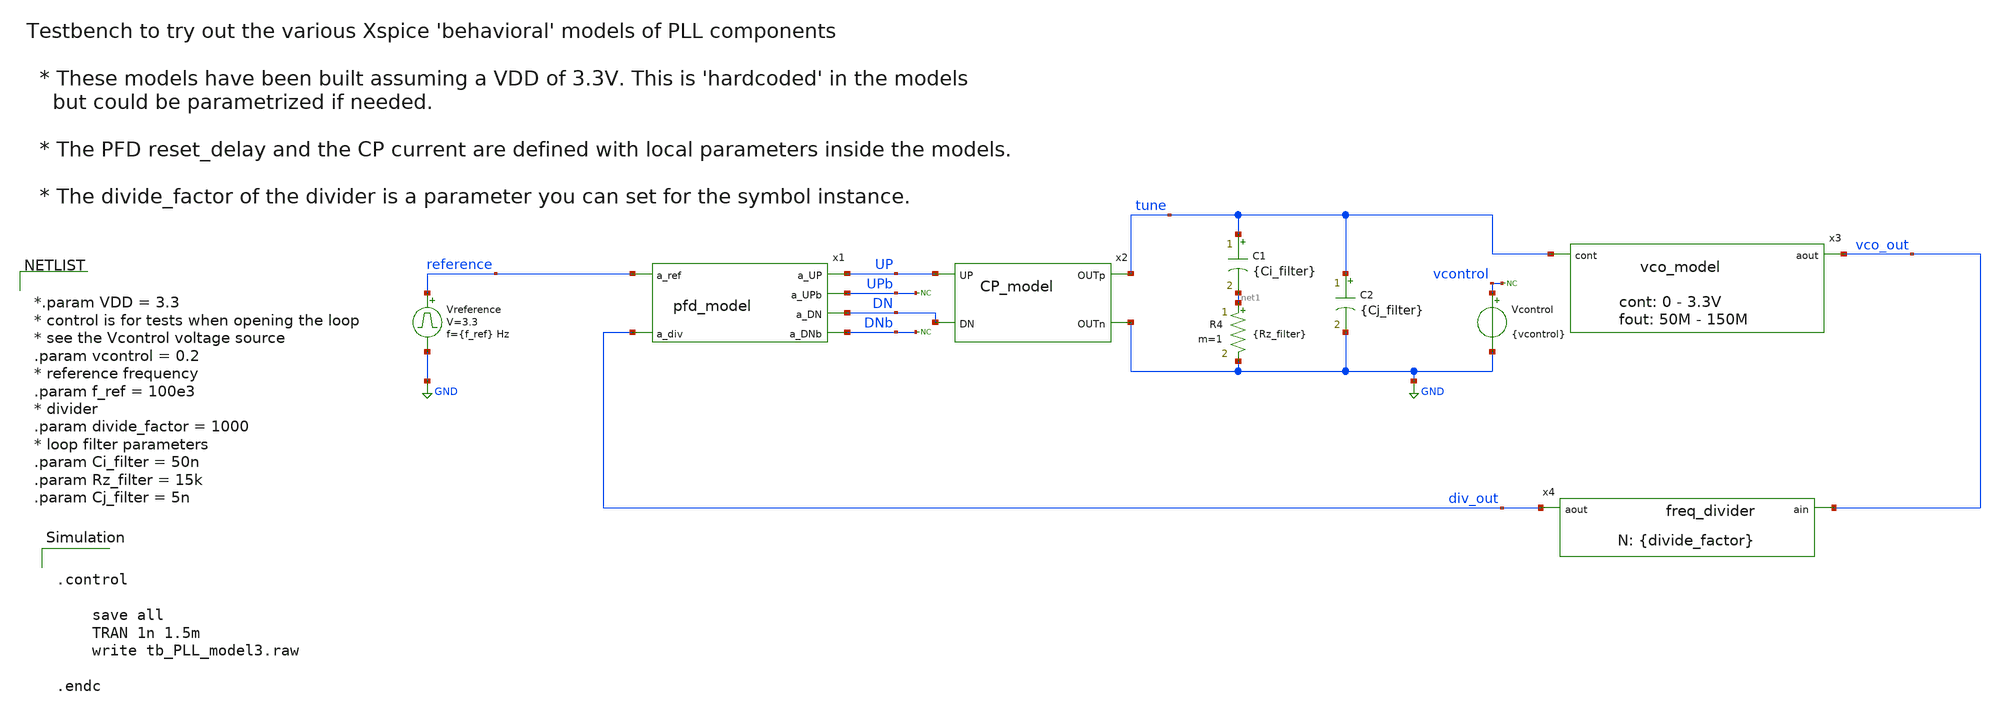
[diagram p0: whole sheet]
** sch_path: designs/libs/tb_pll/tb_PLL_IDEAL_model.sch
**.subckt tb_PLL_IDEAL_model
Vcontrol vcontrol GND {vcontrol}
Vreference reference GND pulse 0 3.3 '0.495/ {f_ref} ' '0.01/{f_ref} ' '0.01/{f_ref} ' '0.49/{f_ref} '
+ '1/{f_ref} '
C1 tune net1 {Ci_filter} m=1
R4 net1 GND {Rz_filter} m=1
* noconn vcontrol
* noconn UPb
* noconn DNb
C2 tune GND {Cj_filter} m=1
x1 reference UP UPb DN div_out DNb pfd_model
x2 tune UP DN GND CP_model
x3 vco_out tune vco_model
x4 div_out vco_out freq_divider divide_factor={divide_factor}
**** begin user architecture code


.control

    save all
    TRAN 1n 1.5m
    write tb_PLL_model3.raw

.endc




*.param VDD = 3.3
* control is for tests when opening the loop
* see the Vcontrol voltage source
.param vcontrol = 0.2
* reference frequency
.param f_ref = 100e3
* divider
.param divide_factor = 1000
* loop filter parameters
.param Ci_filter = 50n
.param Rz_filter = 15k
.param Cj_filter = 5n


**** end user architecture code
**.ends

* expanding   symbol:  libs/model_pll/pfd_model.sym # of pins=6
** sym_path: designs/libs/model_pll/pfd_model.sym
** sch_path: designs/libs/model_pll/pfd_model.sch
.subckt pfd_model a_ref a_UP a_UPb a_DN a_div a_DNb
*.ipin a_ref
*.ipin a_div
*.opin a_UP
*.opin a_UPb
*.opin a_DN
*.opin a_DNb
**** begin user architecture code



* PFD Model using digital Xspice components
*
* At the end we add the necessary a-d and d-a blocks so the
* signals can be put on pins or the internal signals can be
* observed when plotting (the latter is for debugging)

* pfd_delay local parameter sets the duration of the a_UP and a_DN
* signals; it is implemented with the reset_delay of
* the flip flops

.param pfd_delay = 10n

** Digital 1 and 0 to drive Flip-Flops
aone 0 d_d1 d_inv
azero d_d1 d_d0 d_inv
.model d_inv d_inverter()

** Flip Flops
ad1 d_d1 d_R d_d0 d_rset d_U d_U_ flop1
ad2 d_d1 d_V d_d0 d_rset d_D d_D_ flop1
.model flop1 d_dff(clk_delay = 1.0e-10 set_delay = 1.0e-10  reset_delay = {pfd_delay} ic = 2 rise_delay
+ = 1.0e-10  fall_delay = 1e-10)

* AND Gate
aa1 [d_U d_D] d_rset and1
.model and1 d_and(rise_delay = 1e-10 fall_delay = 1e-10  input_load = 0.5e-12)

aADC [ a_ref a_div ] [ d_R d_V ] adc_buff
.model adc_buff adc_bridge(in_low = 1.6 in_high = 1.7)

aDAC [ d_U d_U_ d_D d_D_ d_rset d_R d_V d_d1 d_d0 ] [ a_UP a_UPb a_DN a_DNb a_rset a_R a_V a_d1
+ a_d0] dac_buff
.model dac_buff dac_bridge(out_low = 0 out_high = 3.3)



**** end user architecture code
* noconn a_ref
* noconn a_div
* noconn a_UP
* noconn a_UPb
* noconn a_DN
* noconn a_DNb
.ends


* expanding   symbol:  libs/model_pll/CP_model.sym # of pins=4
** sym_path: designs/libs/model_pll/CP_model.sym
** sch_path: designs/libs/model_pll/CP_model.sch
.subckt CP_model OUTp UP DN OUTn
*.ipin UP
*.ipin DN
*.opin OUTp
*.opin OUTn
G1 OUTn OUTp UP DN {Gm_CP}
**** begin user architecture code


* Charge Pump Model
*

* local parameter Gm_CP sets the charge pump gain
* UP and DN are 0 or 3.3 so for an ICP of 1mA you
* need a Gm of 1m/3.3
*
*
* In single-ended applications, connect the OUTn to ground or VSS
* and the OUTp to the loop filter

.param ICP = 1m
.param VDD = 3.3
.param Gm_CP = {ICP/VDD}



**** end user architecture code
.ends


* expanding   symbol:  libs/model_pll/vco_model.sym # of pins=2
** sym_path: designs/libs/model_pll/vco_model.sym
** sch_path: designs/libs/model_pll/vco_model.sch
.subckt vco_model aout cont
*.ipin cont
*.opin aout
**** begin user architecture code


***** XSPICE analog sine VCO ***************
* 50 MHz to 150 MHz
* aout analog out
* cont control voltage between 0 and 3.3V
* KVCO = (150-50)/(3.3 - 0) MHz/V

asine cont aout analog_sin_osc
.model analog_sin_osc sine(cntl_array = [ 0    3.3 ]                           freq_array = [50e6
+ 150e6]                           out_high = 3.0 out_low = 0.3 )



**** end user architecture code
* noconn aout
* noconn cont
.ends


* expanding   symbol:  libs/model_pll/freq_divider.sym # of pins=2
** sym_path: designs/libs/model_pll/freq_divider.sym
** sch_path: designs/libs/model_pll/freq_divider.sch
.subckt freq_divider aout ain  divide_factor=20
*.ipin ain
*.opin aout
**** begin user architecture code


* Frequency divider model
* This is a digital Xspice component
* so we place an a-d bridge at the input
* and a d-a bridge at the output

* The division factor is a parameter for the subckt
* (check out the symbol for the interface definition)

.param divide_factor = 10

* high_cycles is just a local parameter and makes sure
* that we get a reasonable duty cycle on the divider
* output signal

.param high_cycles = {floor(divide_factor/4)}

adiv din dout divider
.model divider d_fdiv(div_factor = {divide_factor}  high_cycles = {high_cycles}   i_count = 0   rise_delay
+ = 1e-10 fall_delay = 1e-10 )

aADC [ ain ] [ din ] adc_buff
.model adc_buff adc_bridge(in_low = 1.6 in_high = 1.7)

aDAC [ dout ] [ aout ] dac_buff
.model dac_buff dac_bridge(out_low = 0 out_high = 3.3)



**** end user architecture code
* noconn ain
* noconn aout
.ends

.GLOBAL GND
.end
